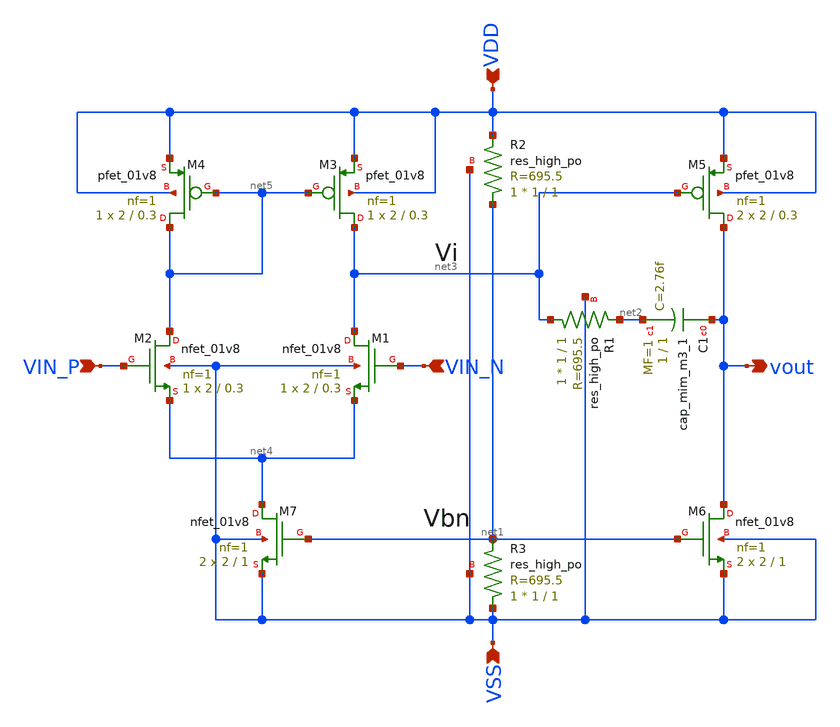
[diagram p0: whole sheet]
** sch_path: analog/schematics/opamp_two_stage.sch
**.subckt opamp_two_stage VIN_P VIN_N vout VDD VSS
*.ipin VIN_P
*.ipin VIN_N
*.opin vout
*.ipin VDD
*.ipin VSS
XM1 net3 VIN_N net4 VSS sky130_fd_pr__nfet_01v8 L=0.3 W=2 nf=1 ad='int((nf+1)/2) * W/nf * 0.29' as='int((nf+2)/2) * W/nf * 0.29'
+ pd='2*int((nf+1)/2) * (W/nf + 0.29)' ps='2*int((nf+2)/2) * (W/nf + 0.29)' nrd='0.29 / W' nrs='0.29 / W'
+ sa=0 sb=0 sd=0 mult=1 m=1
XM2 net5 VIN_P net4 VSS sky130_fd_pr__nfet_01v8 L=0.3 W=2 nf=1 ad='int((nf+1)/2) * W/nf * 0.29' as='int((nf+2)/2) * W/nf * 0.29'
+ pd='2*int((nf+1)/2) * (W/nf + 0.29)' ps='2*int((nf+2)/2) * (W/nf + 0.29)' nrd='0.29 / W' nrs='0.29 / W'
+ sa=0 sb=0 sd=0 mult=1 m=1
XM3 net3 net5 VDD VDD sky130_fd_pr__pfet_01v8 L=0.3 W=2 nf=1 ad='int((nf+1)/2) * W/nf * 0.29' as='int((nf+2)/2) * W/nf * 0.29'
+ pd='2*int((nf+1)/2) * (W/nf + 0.29)' ps='2*int((nf+2)/2) * (W/nf + 0.29)' nrd='0.29 / W' nrs='0.29 / W'
+ sa=0 sb=0 sd=0 mult=1 m=1
XM4 net5 net5 VDD VDD sky130_fd_pr__pfet_01v8 L=0.3 W=2 nf=1 ad='int((nf+1)/2) * W/nf * 0.29' as='int((nf+2)/2) * W/nf * 0.29'
+ pd='2*int((nf+1)/2) * (W/nf + 0.29)' ps='2*int((nf+2)/2) * (W/nf + 0.29)' nrd='0.29 / W' nrs='0.29 / W'
+ sa=0 sb=0 sd=0 mult=1 m=1
XM5 vout net3 VDD VDD sky130_fd_pr__pfet_01v8 L=0.3 W=2 nf=1 ad='int((nf+1)/2) * W/nf * 0.29' as='int((nf+2)/2) * W/nf * 0.29'
+ pd='2*int((nf+1)/2) * (W/nf + 0.29)' ps='2*int((nf+2)/2) * (W/nf + 0.29)' nrd='0.29 / W' nrs='0.29 / W'
+ sa=0 sb=0 sd=0 mult=2 m=2
XM6 vout net1 VSS VSS sky130_fd_pr__nfet_01v8 L=1 W=2 nf=1 ad='int((nf+1)/2) * W/nf * 0.29' as='int((nf+2)/2) * W/nf * 0.29'
+ pd='2*int((nf+1)/2) * (W/nf + 0.29)' ps='2*int((nf+2)/2) * (W/nf + 0.29)' nrd='0.29 / W' nrs='0.29 / W'
+ sa=0 sb=0 sd=0 mult=2 m=2
XM7 net4 net1 VSS VSS sky130_fd_pr__nfet_01v8 L=1 W=2 nf=1 ad='int((nf+1)/2) * W/nf * 0.29' as='int((nf+2)/2) * W/nf * 0.29'
+ pd='2*int((nf+1)/2) * (W/nf + 0.29)' ps='2*int((nf+2)/2) * (W/nf + 0.29)' nrd='0.29 / W' nrs='0.29 / W'
+ sa=0 sb=0 sd=0 mult=2 m=2
XR1 net3 net2 VSS sky130_fd_pr__res_high_po W=1 L=1 mult=1 m=1
XC1 vout net2 sky130_fd_pr__cap_mim_m3_1 W=1 L=1 MF=1 m=1
XR2 net1 VDD VSS sky130_fd_pr__res_high_po W=1 L=1 mult=1 m=1
XR3 VSS net1 VSS sky130_fd_pr__res_high_po W=1 L=1 mult=1 m=1
**.ends
.end
